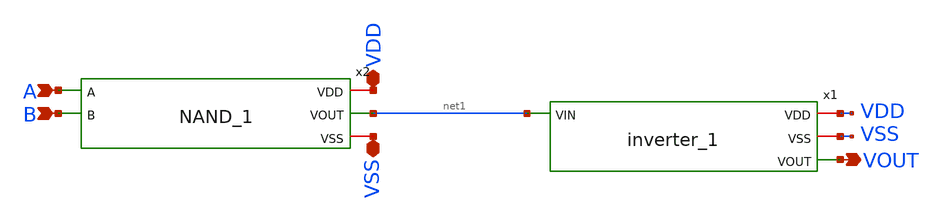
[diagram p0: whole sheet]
** sch_path: Xschem/PLL_TOP_Schematics/AND.sch
**.subckt AND VDD VSS A B VOUT
*.iopin VDD
*.iopin VSS
*.ipin A
*.ipin B
*.opin VOUT
x1 VDD VSS VOUT net1 inverter_1
x2 VDD net1 A B VSS NAND_1
**.ends

* expanding   symbol:  inverter_1.sym # of pins=4
** sym_path: Xschem/PLL_TOP_Schematics/inverter_1.sym
** sch_path: Xschem/PLL_TOP_Schematics/inverter_1.sch
.subckt inverter_1 VDD VSS VOUT VIN
*.opin VOUT
*.iopin VSS
*.iopin VDD
*.ipin VIN
XM3 VOUT VIN VDD VDD sky130_fd_pr__pfet_01v8 L=0.2 W=3 nf=1 ad='int((nf+1)/2) * W/nf * 0.29' as='int((nf+2)/2) * W/nf * 0.29'
+ pd='2*int((nf+1)/2) * (W/nf + 0.29)' ps='2*int((nf+2)/2) * (W/nf + 0.29)' nrd='0.29 / W' nrs='0.29 / W'
+ sa=0 sb=0 sd=0 mult=1 m=1
XM5 VOUT VIN VSS VSS sky130_fd_pr__nfet_01v8 L=0.2 W=1.5 nf=1 ad='int((nf+1)/2) * W/nf * 0.29' as='int((nf+2)/2) * W/nf * 0.29'
+ pd='2*int((nf+1)/2) * (W/nf + 0.29)' ps='2*int((nf+2)/2) * (W/nf + 0.29)' nrd='0.29 / W' nrs='0.29 / W'
+ sa=0 sb=0 sd=0 mult=1 m=1
.ends


* expanding   symbol:  NAND_1.sym # of pins=5
** sym_path: Xschem/PLL_TOP_Schematics/NAND_1.sym
** sch_path: Xschem/PLL_TOP_Schematics/NAND_1.sch
.subckt NAND_1 VDD VOUT A B VSS
*.iopin VDD
*.iopin VSS
*.ipin A
*.ipin B
*.opin VOUT
XM1 VOUT A net1 VSS sky130_fd_pr__nfet_01v8 L=0.2 W=3 nf=1 ad='int((nf+1)/2) * W/nf * 0.29' as='int((nf+2)/2) * W/nf * 0.29'
+ pd='2*int((nf+1)/2) * (W/nf + 0.29)' ps='2*int((nf+2)/2) * (W/nf + 0.29)' nrd='0.29 / W' nrs='0.29 / W'
+ sa=0 sb=0 sd=0 mult=1 m=1
XM2 net1 B VSS VSS sky130_fd_pr__nfet_01v8 L=0.2 W=3 nf=1 ad='int((nf+1)/2) * W/nf * 0.29' as='int((nf+2)/2) * W/nf * 0.29'
+ pd='2*int((nf+1)/2) * (W/nf + 0.29)' ps='2*int((nf+2)/2) * (W/nf + 0.29)' nrd='0.29 / W' nrs='0.29 / W'
+ sa=0 sb=0 sd=0 mult=1 m=1
XM6 VOUT B VDD VDD sky130_fd_pr__pfet_01v8 L=0.2 W=3 nf=1 ad='int((nf+1)/2) * W/nf * 0.29' as='int((nf+2)/2) * W/nf * 0.29'
+ pd='2*int((nf+1)/2) * (W/nf + 0.29)' ps='2*int((nf+2)/2) * (W/nf + 0.29)' nrd='0.29 / W' nrs='0.29 / W'
+ sa=0 sb=0 sd=0 mult=1 m=1
XM7 VOUT A VDD VDD sky130_fd_pr__pfet_01v8 L=0.2 W=3 nf=1 ad='int((nf+1)/2) * W/nf * 0.29' as='int((nf+2)/2) * W/nf * 0.29'
+ pd='2*int((nf+1)/2) * (W/nf + 0.29)' ps='2*int((nf+2)/2) * (W/nf + 0.29)' nrd='0.29 / W' nrs='0.29 / W'
+ sa=0 sb=0 sd=0 mult=1 m=1
.ends

.end
